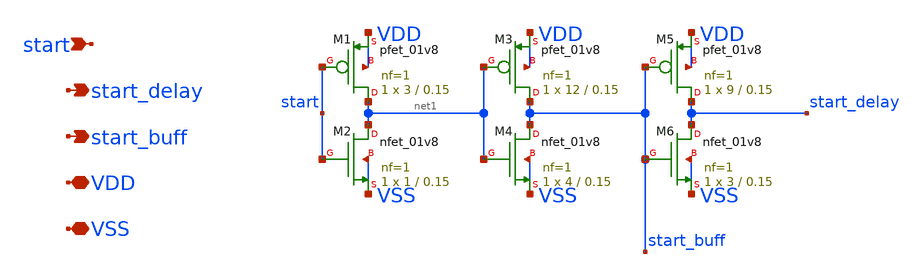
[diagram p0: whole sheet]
** sch_path: xschem/start_buffer.sch
**.subckt start_buffer VDD VSS start start_delay start_buff
*.iopin VDD
*.iopin VSS
*.ipin start
*.opin start_delay
*.opin start_buff
XM1 net1 start VDD VDD sky130_fd_pr__pfet_01v8 L=0.15 W=3 nf=1 ad='int((nf+1)/2) * W/nf * 0.29' as='int((nf+2)/2) * W/nf * 0.29'
+ pd='2*int((nf+1)/2) * (W/nf + 0.29)' ps='2*int((nf+2)/2) * (W/nf + 0.29)' nrd='0.29 / W' nrs='0.29 / W'
+ sa=0 sb=0 sd=0 mult=1 m=1
XM2 net1 start VSS VSS sky130_fd_pr__nfet_01v8 L=0.15 W=1 nf=1 ad='int((nf+1)/2) * W/nf * 0.29' as='int((nf+2)/2) * W/nf * 0.29'
+ pd='2*int((nf+1)/2) * (W/nf + 0.29)' ps='2*int((nf+2)/2) * (W/nf + 0.29)' nrd='0.29 / W' nrs='0.29 / W'
+ sa=0 sb=0 sd=0 mult=1 m=1
XM3 start_buff net1 VDD VDD sky130_fd_pr__pfet_01v8 L=0.15 W=12 nf=1 ad='int((nf+1)/2) * W/nf * 0.29'
+ as='int((nf+2)/2) * W/nf * 0.29' pd='2*int((nf+1)/2) * (W/nf + 0.29)' ps='2*int((nf+2)/2) * (W/nf + 0.29)'
+ nrd='0.29 / W' nrs='0.29 / W' sa=0 sb=0 sd=0 mult=1 m=1
XM4 start_buff net1 VSS VSS sky130_fd_pr__nfet_01v8 L=0.15 W=4 nf=1 ad='int((nf+1)/2) * W/nf * 0.29'
+ as='int((nf+2)/2) * W/nf * 0.29' pd='2*int((nf+1)/2) * (W/nf + 0.29)' ps='2*int((nf+2)/2) * (W/nf + 0.29)'
+ nrd='0.29 / W' nrs='0.29 / W' sa=0 sb=0 sd=0 mult=1 m=1
XM5 start_delay start_buff VDD VDD sky130_fd_pr__pfet_01v8 L=0.15 W=9 nf=1 ad='int((nf+1)/2) * W/nf * 0.29'
+ as='int((nf+2)/2) * W/nf * 0.29' pd='2*int((nf+1)/2) * (W/nf + 0.29)' ps='2*int((nf+2)/2) * (W/nf + 0.29)'
+ nrd='0.29 / W' nrs='0.29 / W' sa=0 sb=0 sd=0 mult=1 m=1
XM6 start_delay start_buff VSS VSS sky130_fd_pr__nfet_01v8 L=0.15 W=3 nf=1 ad='int((nf+1)/2) * W/nf * 0.29'
+ as='int((nf+2)/2) * W/nf * 0.29' pd='2*int((nf+1)/2) * (W/nf + 0.29)' ps='2*int((nf+2)/2) * (W/nf + 0.29)'
+ nrd='0.29 / W' nrs='0.29 / W' sa=0 sb=0 sd=0 mult=1 m=1
**.ends
.end
